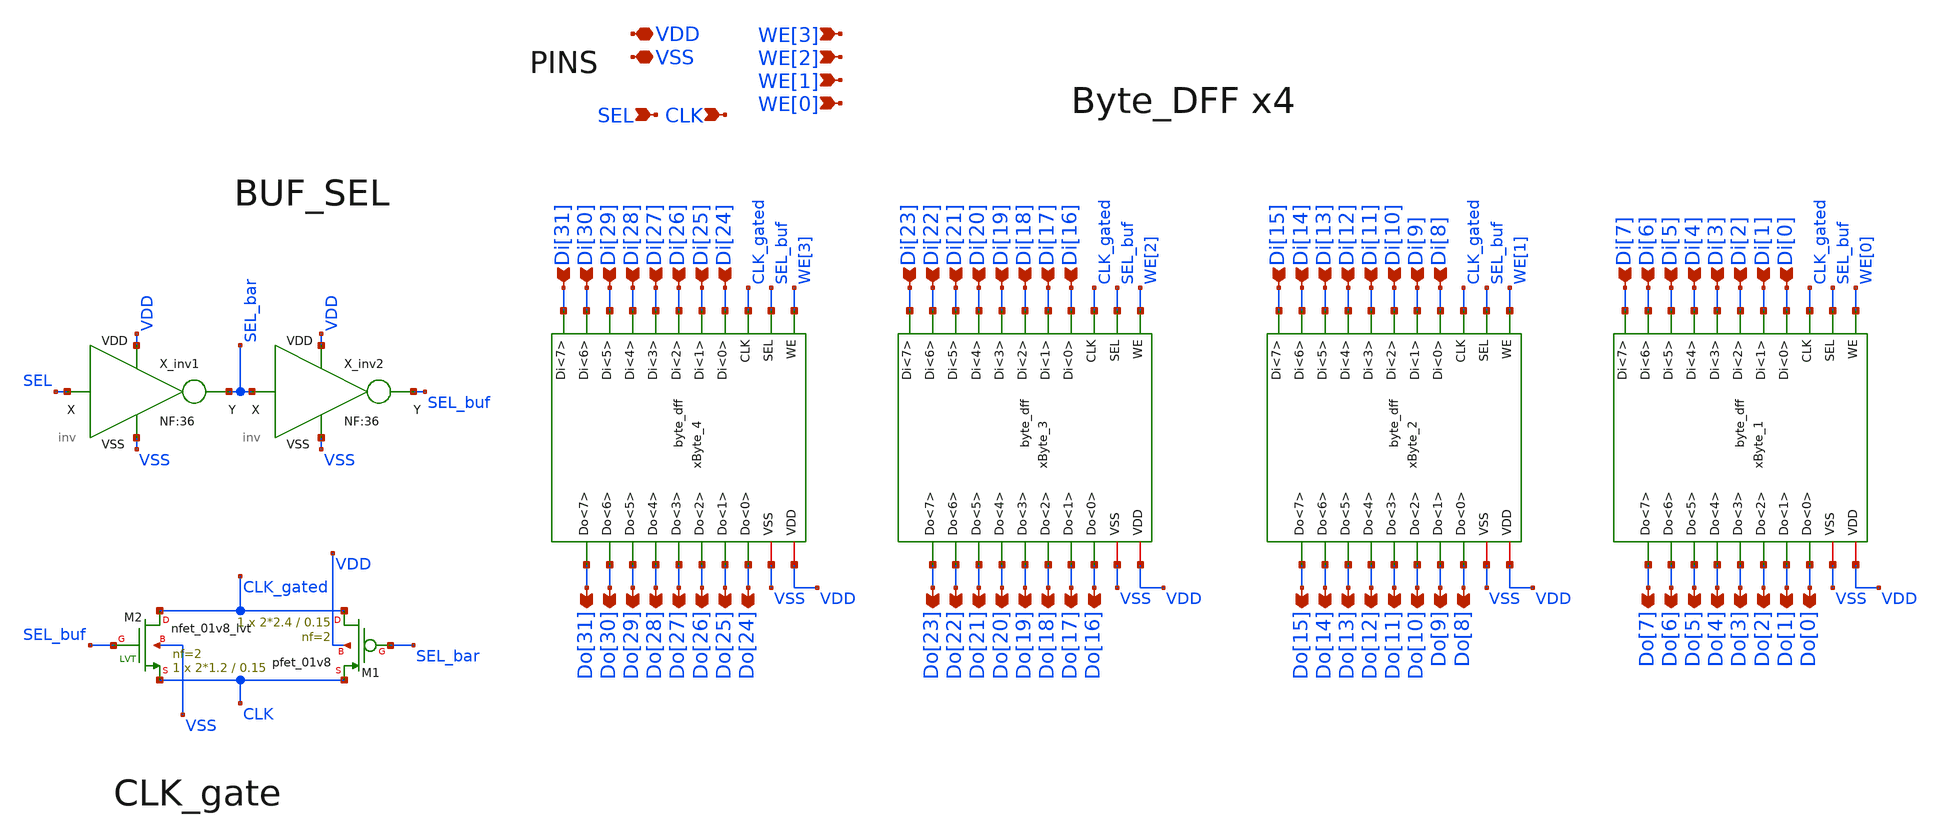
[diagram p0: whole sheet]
** sch_path: xschem_lib/DFFRAM_full_custom/word.sch
**.subckt word SEL WE[0] Di[31] Di[30] Di[29] Di[28] Di[27] Di[26] Di[25] Di[24] Do[31] Do[30]
*+ Do[29] Do[28] Do[27] Do[26] Do[25] Do[24] VDD VSS Di[23] Di[22] Di[21] Di[20] Di[19] Di[18] Di[17] Di[16]
*+ Do[23] Do[22] Do[21] Do[20] Do[19] Do[18] Do[17] Do[16] Di[15] Di[14] Di[13] Di[12] Di[11] Di[10] Di[9]
*+ Di[8] Do[15] Do[14] Do[13] Do[12] Do[11] Do[10] Do[9] Do[8] Di[7] Di[6] Di[5] Di[4] Di[3] Di[2] Di[1]
*+ Di[0] Do[7] Do[6] Do[5] Do[4] Do[3] Do[2] Do[1] Do[0] WE[1] WE[2] WE[3] CLK
*.ipin SEL
*.ipin WE[0]
*.ipin Di[31]
*.ipin Di[30]
*.ipin Di[29]
*.ipin Di[28]
*.ipin Di[27]
*.ipin Di[26]
*.ipin Di[25]
*.ipin Di[24]
*.opin Do[31]
*.opin Do[30]
*.opin Do[29]
*.opin Do[28]
*.opin Do[27]
*.opin Do[26]
*.opin Do[25]
*.opin Do[24]
*.iopin VDD
*.iopin VSS
*.ipin Di[23]
*.ipin Di[22]
*.ipin Di[21]
*.ipin Di[20]
*.ipin Di[19]
*.ipin Di[18]
*.ipin Di[17]
*.ipin Di[16]
*.opin Do[23]
*.opin Do[22]
*.opin Do[21]
*.opin Do[20]
*.opin Do[19]
*.opin Do[18]
*.opin Do[17]
*.opin Do[16]
*.ipin Di[15]
*.ipin Di[14]
*.ipin Di[13]
*.ipin Di[12]
*.ipin Di[11]
*.ipin Di[10]
*.ipin Di[9]
*.ipin Di[8]
*.opin Do[15]
*.opin Do[14]
*.opin Do[13]
*.opin Do[12]
*.opin Do[11]
*.opin Do[10]
*.opin Do[9]
*.opin Do[8]
*.ipin Di[7]
*.ipin Di[6]
*.ipin Di[5]
*.ipin Di[4]
*.ipin Di[3]
*.ipin Di[2]
*.ipin Di[1]
*.ipin Di[0]
*.opin Do[7]
*.opin Do[6]
*.opin Do[5]
*.opin Do[4]
*.opin Do[3]
*.opin Do[2]
*.opin Do[1]
*.opin Do[0]
*.ipin WE[1]
*.ipin WE[2]
*.ipin WE[3]
*.ipin CLK
xByte_1 VDD VSS WE[0] Di[3] Di[7] Do[3] Do[7] CLK_gated SEL_buf Di[2] Di[6] Do[2] Do[6] Di[5] Di[1]
+ Do[5] Do[1] Di[4] Do[4] Di[0] Do[0] byte_dff NF=2
X_inv1 SEL VDD VSS SEL_bar inv NF=36
X_inv2 SEL_bar VDD VSS SEL_buf inv NF=36
xByte_2 VDD VSS WE[1] Di[11] Di[15] Do[11] Do[15] CLK_gated SEL_buf Di[10] Di[14] Do[10] Do[14]
+ Di[13] Di[9] Do[13] Do[9] Di[12] Do[12] Di[8] Do[8] byte_dff NF=2
xByte_3 VDD VSS WE[2] Di[19] Di[23] Do[19] Do[23] CLK_gated SEL_buf Di[18] Di[22] Do[18] Do[22]
+ Di[21] Di[17] Do[21] Do[17] Di[20] Do[20] Di[16] Do[16] byte_dff NF=2
xByte_4 VDD VSS WE[3] Di[27] Di[31] Do[27] Do[31] CLK_gated SEL_buf Di[26] Di[30] Do[26] Do[30]
+ Di[29] Di[25] Do[29] Do[25] Di[28] Do[28] Di[24] Do[24] byte_dff NF=2
XM1 CLK_gated SEL_bar CLK VDD sky130_fd_pr__pfet_01v8 L=0.15 W=2*2.4 nf=2 ad='int((nf+1)/2) * W/nf * 0.29'
+ as='int((nf+2)/2) * W/nf * 0.29' pd='2*int((nf+1)/2) * (W/nf + 0.29)' ps='2*int((nf+2)/2) * (W/nf + 0.29)'
+ nrd='0.29 / W' nrs='0.29 / W' sa=0 sb=0 sd=0 mult=1 m=1
XM2 CLK_gated SEL_buf CLK VSS sky130_fd_pr__nfet_01v8_lvt L=0.15 W=2*1.2 nf=2 ad='int((nf+1)/2) * W/nf * 0.29'
+ as='int((nf+2)/2) * W/nf * 0.29' pd='2*int((nf+1)/2) * (W/nf + 0.29)' ps='2*int((nf+2)/2) * (W/nf + 0.29)'
+ nrd='0.29 / W' nrs='0.29 / W' sa=0 sb=0 sd=0 mult=1 m=1
**.ends
.end
